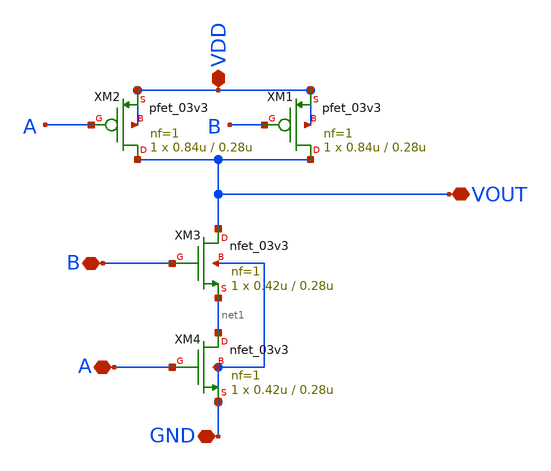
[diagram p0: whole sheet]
** sch_path: src/pixel/NAND.sch
**.subckt NAND A B GND VDD VOUT
*.iopin A
*.iopin B
*.iopin GND
*.iopin VDD
*.iopin VOUT
XM1 VOUT B VDD VDD pfet_03v3 L=0.28u W=0.84u nf=1 ad='int((nf+1)/2) * W/nf * 0.18u' as='int((nf+2)/2) * W/nf * 0.18u'
+ pd='2*int((nf+1)/2) * (W/nf + 0.18u)' ps='2*int((nf+2)/2) * (W/nf + 0.18u)' nrd='0.18u / W' nrs='0.18u / W'
+ sa=0 sb=0 sd=0 m=1
XM2 VOUT A VDD VDD pfet_03v3 L=0.28u W=0.84u nf=1 ad='int((nf+1)/2) * W/nf * 0.18u' as='int((nf+2)/2) * W/nf * 0.18u'
+ pd='2*int((nf+1)/2) * (W/nf + 0.18u)' ps='2*int((nf+2)/2) * (W/nf + 0.18u)' nrd='0.18u / W' nrs='0.18u / W'
+ sa=0 sb=0 sd=0 m=1
XM3 VOUT B net1 GND nfet_03v3 L=0.28u W=0.42u nf=1 ad='int((nf+1)/2) * W/nf * 0.18u' as='int((nf+2)/2) * W/nf * 0.18u'
+ pd='2*int((nf+1)/2) * (W/nf + 0.18u)' ps='2*int((nf+2)/2) * (W/nf + 0.18u)' nrd='0.18u / W' nrs='0.18u / W'
+ sa=0 sb=0 sd=0 m=1
XM4 net1 A GND GND nfet_03v3 L=0.28u W=0.42u nf=1 ad='int((nf+1)/2) * W/nf * 0.18u' as='int((nf+2)/2) * W/nf * 0.18u'
+ pd='2*int((nf+1)/2) * (W/nf + 0.18u)' ps='2*int((nf+2)/2) * (W/nf + 0.18u)' nrd='0.18u / W' nrs='0.18u / W'
+ sa=0 sb=0 sd=0 m=1
**.ends
.end
